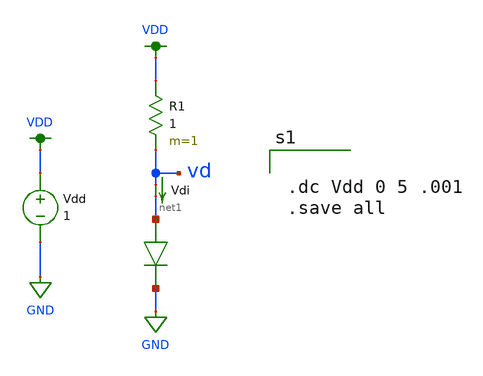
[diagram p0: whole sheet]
** sch_path: schematics/old/diode_schottky_test.sch
**.subckt diode_schottky_test
Vdd VDD GND 1
R1 VDD vd 1 m=1
D1 net1 GND diode_schottky
Vdi vd net1 0
.save i(vdi)
**** begin user architecture code


.dc Vdd 0 5 .001
.save all



*SRC=SBR10U40CT;DI_SBR10U40CT;Diodes;Si;  40.0V  5.00A  35.0ns   Diodes INC SBR rectifier
.model diode_schottky d ( IS=6.83m RS=6.69u BV=40.0 IBV=0.100 CJO=593p  M=0.333 N=7.19 TT=50.4n )

**** end user architecture code
**.ends
.GLOBAL VDD
.GLOBAL GND
.end
